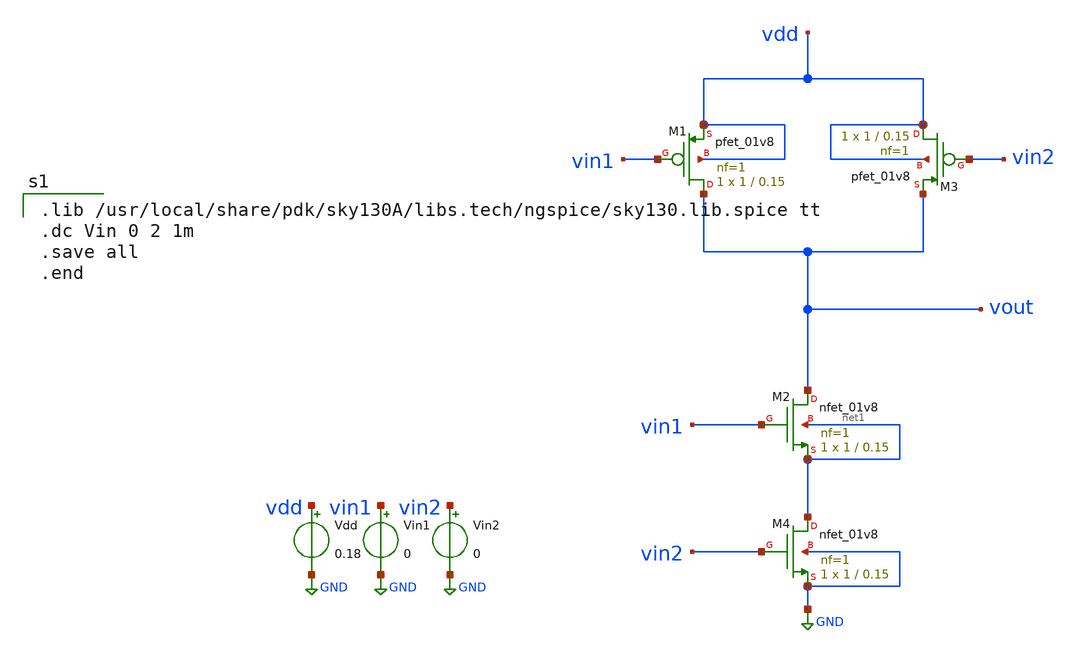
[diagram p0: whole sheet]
** sch_path: nandgate.sch
**.subckt nandgate
XM1 vout vin1 vdd vdd sky130_fd_pr__pfet_01v8 L=0.15 W=1 nf=1 ad='int((1 + 1)/2) * 1 / 1 * 0.29' as='int((1 + 2)/2) * 1 / 1 * 0.29'
+ pd='2*int((1 + 1)/2) * (1 / 1 + 0.29)' ps='2*int((1 + 2)/2) * (1 / 1 + 0.29)' nrd='0.29 / 1 ' nrs='0.29 / 1 '
+ sa=0 sb=0 sd=0 mult=1 m=1
XM2 vout vin1 net1 net1 sky130_fd_pr__nfet_01v8 L=0.15 W=1 nf=1 ad='int((1 + 1)/2) * 1 / 1 * 0.29' as='int((1 + 2)/2) * 1 / 1 * 0.29'
+ pd='2*int((1 + 1)/2) * (1 / 1 + 0.29)' ps='2*int((1 + 2)/2) * (1 / 1 + 0.29)' nrd='0.29 / 1 ' nrs='0.29 / 1 '
+ sa=0 sb=0 sd=0 mult=1 m=1
XM3 vdd vin2 vout vdd sky130_fd_pr__pfet_01v8 L=0.15 W=1 nf=1 ad='int((1 + 1)/2) * 1 / 1 * 0.29' as='int((1 + 2)/2) * 1 / 1 * 0.29'
+ pd='2*int((1 + 1)/2) * (1 / 1 + 0.29)' ps='2*int((1 + 2)/2) * (1 / 1 + 0.29)' nrd='0.29 / 1 ' nrs='0.29 / 1 '
+ sa=0 sb=0 sd=0 mult=1 m=1
XM4 net1 vin2 GND GND sky130_fd_pr__nfet_01v8 L=0.15 W=1 nf=1 ad='int((1 + 1)/2) * 1 / 1 * 0.29' as='int((1 + 2)/2) * 1 / 1 * 0.29'
+ pd='2*int((1 + 1)/2) * (1 / 1 + 0.29)' ps='2*int((1 + 2)/2) * (1 / 1 + 0.29)' nrd='0.29 / 1 ' nrs='0.29 / 1 '
+ sa=0 sb=0 sd=0 mult=1 m=1
Vdd vdd GND 0.18
Vin1 vin1 GND 0
Vin2 vin2 GND 0
**** begin user architecture code

.lib /usr/local/share/pdk/sky130A/libs.tech/ngspice/sky130.lib.spice tt
.dc Vin 0 2 1m
.save all
.end

**** end user architecture code
**.ends
.GLOBAL GND
.end
